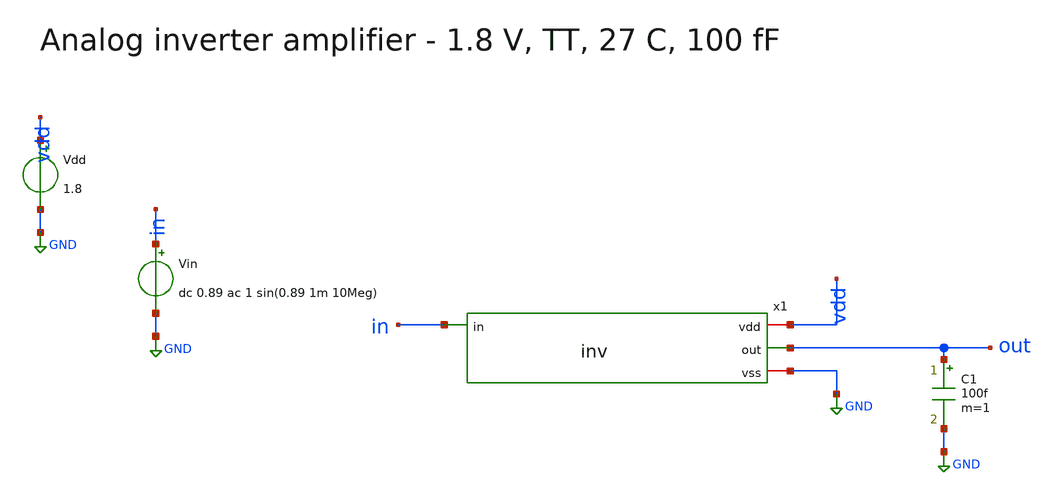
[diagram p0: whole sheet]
** sch_path: ISSCC27/submitted_notebooks/PerfPDN/examples/inverter_amplifier/inverter_access_tb.sch
**.subckt inverter_access_tb
C1 out GND 100f m=1
Vdd vdd GND 1.8
Vin in GND dc 0.89 ac 1 sin(0.89 1m 10Meg)
x1 vdd in out GND inv
**** begin user architecture code

.lib $::SKYWATER_MODELS/sky130.lib.spice tt



.option scale=1e-6
.temp 27
.control
set wr_singlescale
set wr_vecnames
op
print v(in) v(out) i(Vdd)
ac dec 50 1k 100G
let gain_db=db(v(out))
wrdata analog_ac.txt gain_db
tran 500p 600n
let isupply=-i(Vdd)
meas tran iavg AVG isupply from=400n to=600n
wrdata analog_signal.txt v(in) v(out) isupply
.endc


**** end user architecture code
**.ends

* expanding   symbol:  inv.sym # of pins=4
** sym_path: ISSCC27/submitted_notebooks/PerfPDN/examples/inverter_amplifier/inv.sym
** sch_path: ISSCC27/submitted_notebooks/PerfPDN/examples/inverter_amplifier/inv.sch
.subckt inv vdd in out vss
*.ipin in
*.opin out
*.iopin vdd
*.iopin vss
XM1 out in vdd vdd sky130_fd_pr__pfet_01v8 L=0.15 W=6.325 nf=1 ad='int(( 1 + 1 ) / 2 ) * 6.325 / 1 * 0.29'
+ as='int(( 1 + 2 ) / 2 ) * 6.325 / 1 * 0.29' pd='2 * int(( 1 + 1 ) / 2 ) * ( 6.325 / 1 + 0.29 )' ps='2 * int(( 1 + 2 ) / 2 ) * ( 6.325 / 1 + 0.29 )'
+ nrd='0.29 / 6.325 ' nrs='0.29 / 6.325 ' sa=0 sb=0 sd=0 mult=1 m=1
XM2 out in vss vss sky130_fd_pr__nfet_01v8 L=0.15 W=1.67 nf=1 ad='int(( 1 + 1 ) / 2 ) * 1.67 / 1 * 0.29'
+ as='int(( 1 + 2 ) / 2 ) * 1.67 / 1 * 0.29' pd='2 * int(( 1 + 1 ) / 2 ) * ( 1.67 / 1 + 0.29 )' ps='2 * int(( 1 + 2 ) / 2 ) * ( 1.67 / 1 + 0.29 )'
+ nrd='0.29 / 1.67 ' nrs='0.29 / 1.67 ' sa=0 sb=0 sd=0 mult=1 m=1
.ends

.GLOBAL GND
.end
